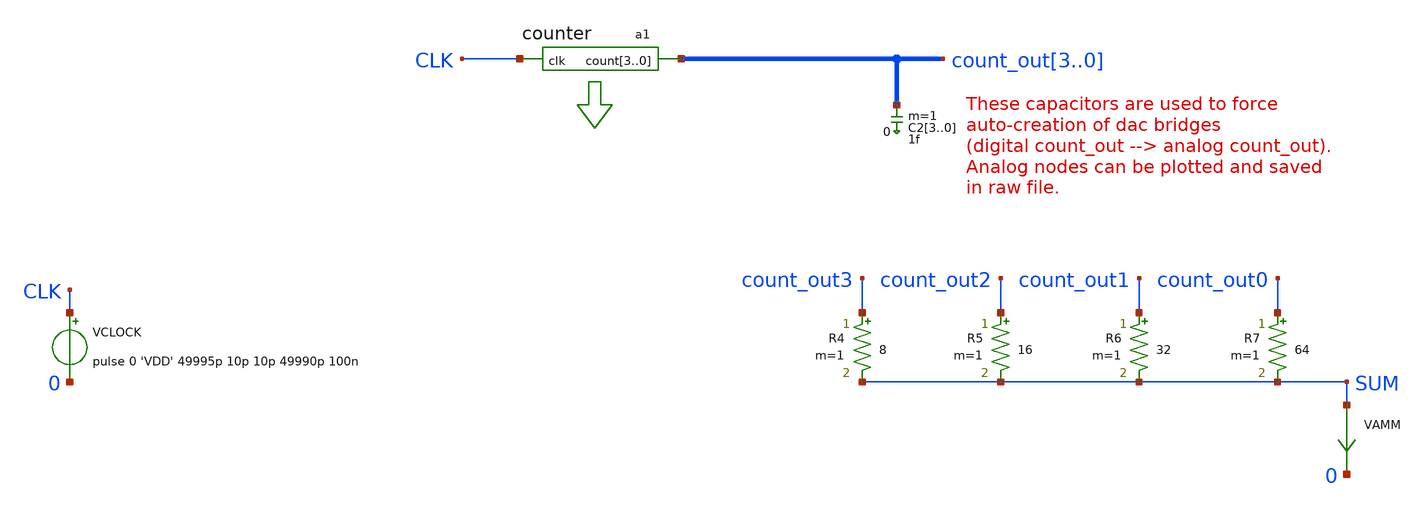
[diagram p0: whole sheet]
** sch_path: xschem_libraries_oa/ngspice_verilog_cosim_ase/tb_counter_wrapper/schematic/tb_counter_wrapper.sch
**.subckt tb_counter_wrapper
VCLOCK CLK 0 pulse 0 'VDD' 49995p 10p 10p 49990p 100n
a1 [ CLK ] [ count_out3 count_out2 count_out1 count_out0 ] counter
C23 count_out3 0 1f m=1
C22 count_out2 0 1f m=1
C21 count_out1 0 1f m=1
C20 count_out0 0 1f m=1
VAMM SUM 0 0
R4 count_out3 SUM 8 m=1
R5 count_out2 SUM 16 m=1
R6 count_out1 SUM 32 m=1
R7 count_out0 SUM 64 m=1
**.ends
**** begin user architecture code
.model counter d_cosim simulation="./counter.so" sim_args=["counter.vcd"] delay=0
**** end user architecture code
.end
